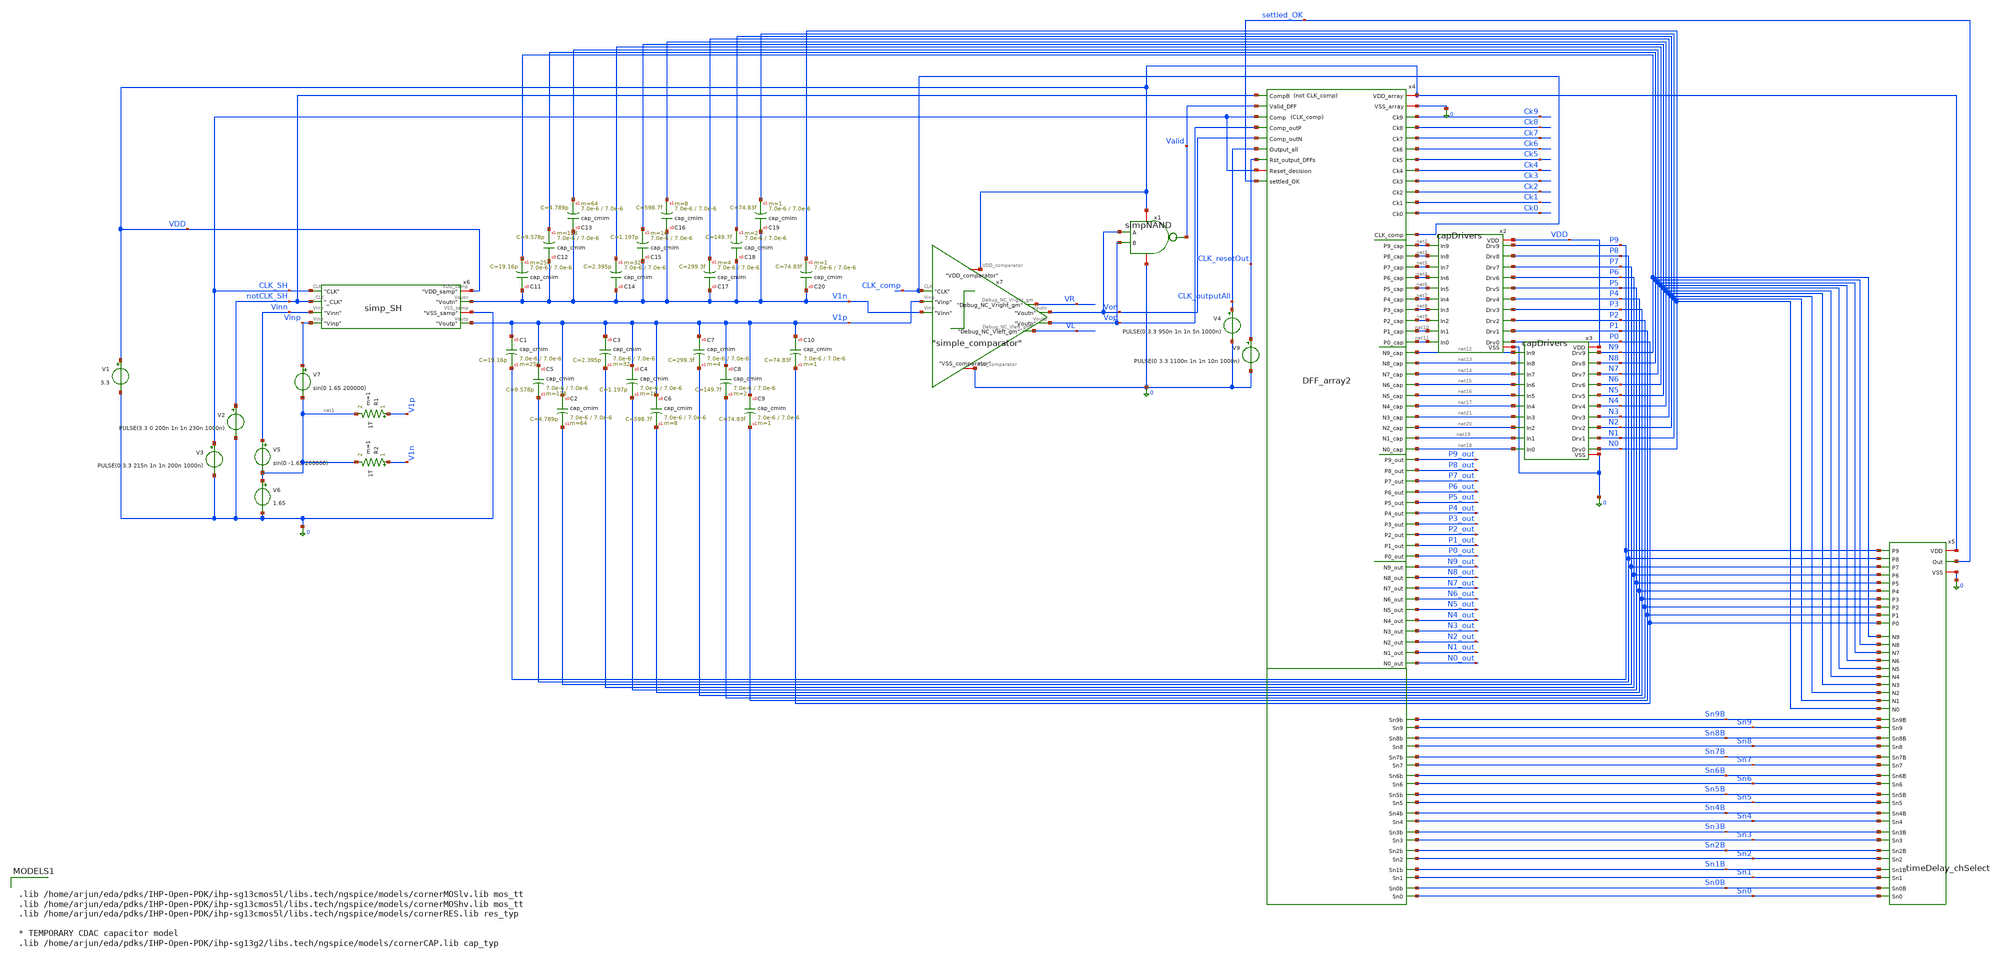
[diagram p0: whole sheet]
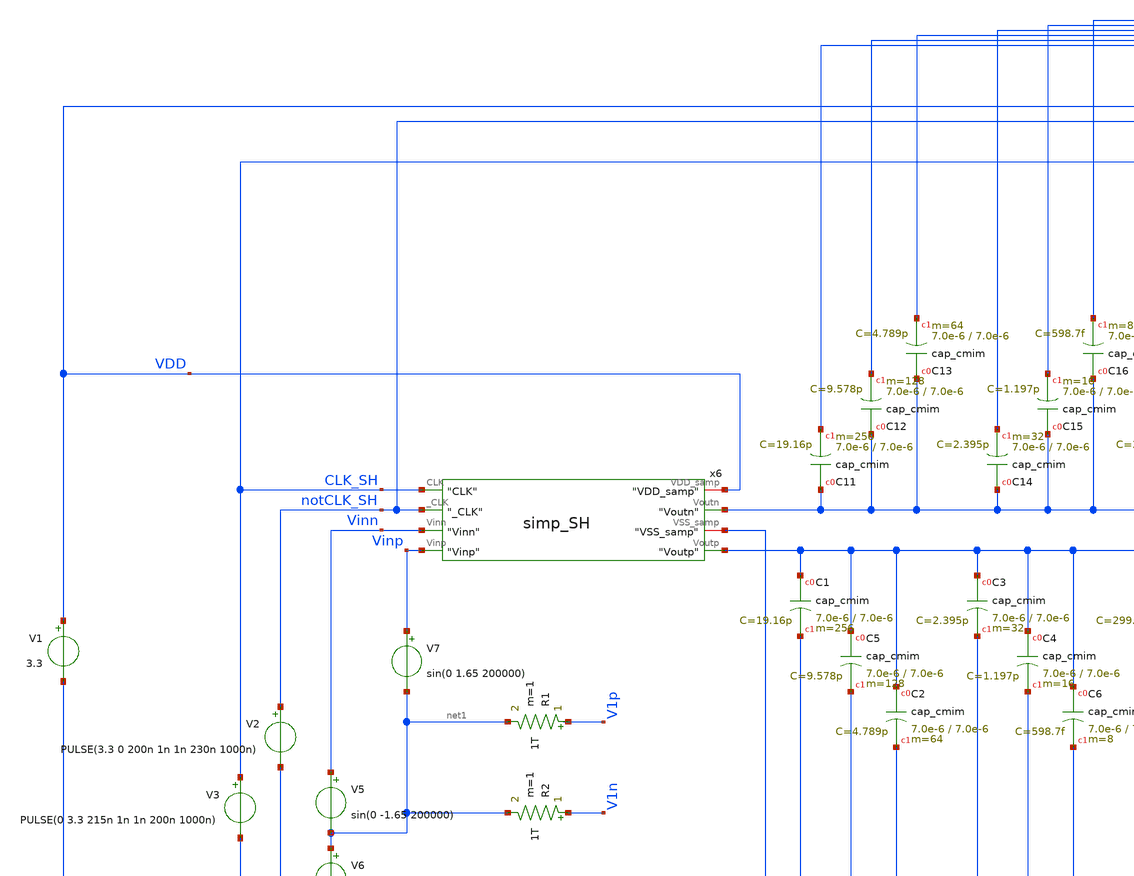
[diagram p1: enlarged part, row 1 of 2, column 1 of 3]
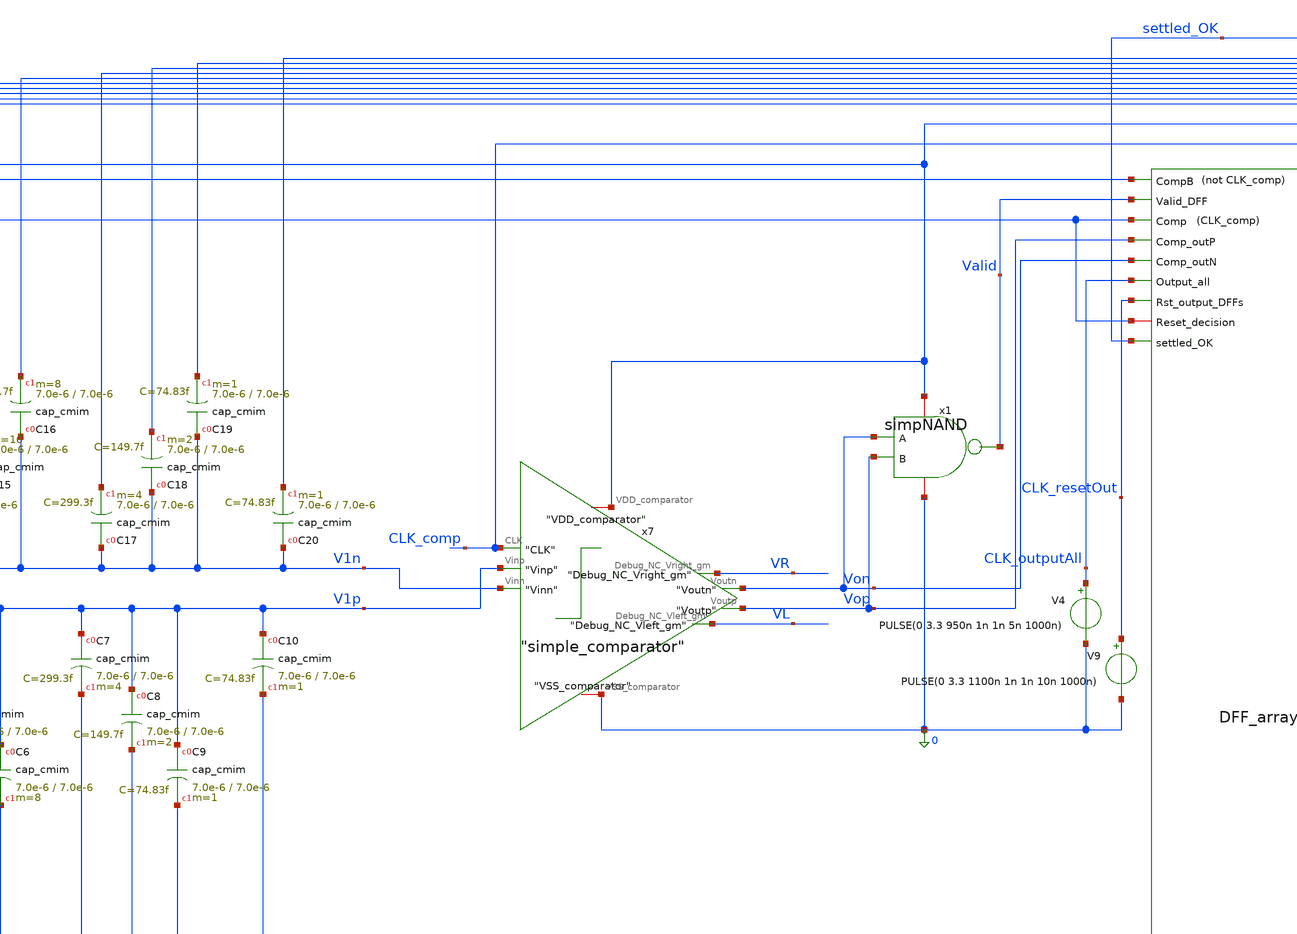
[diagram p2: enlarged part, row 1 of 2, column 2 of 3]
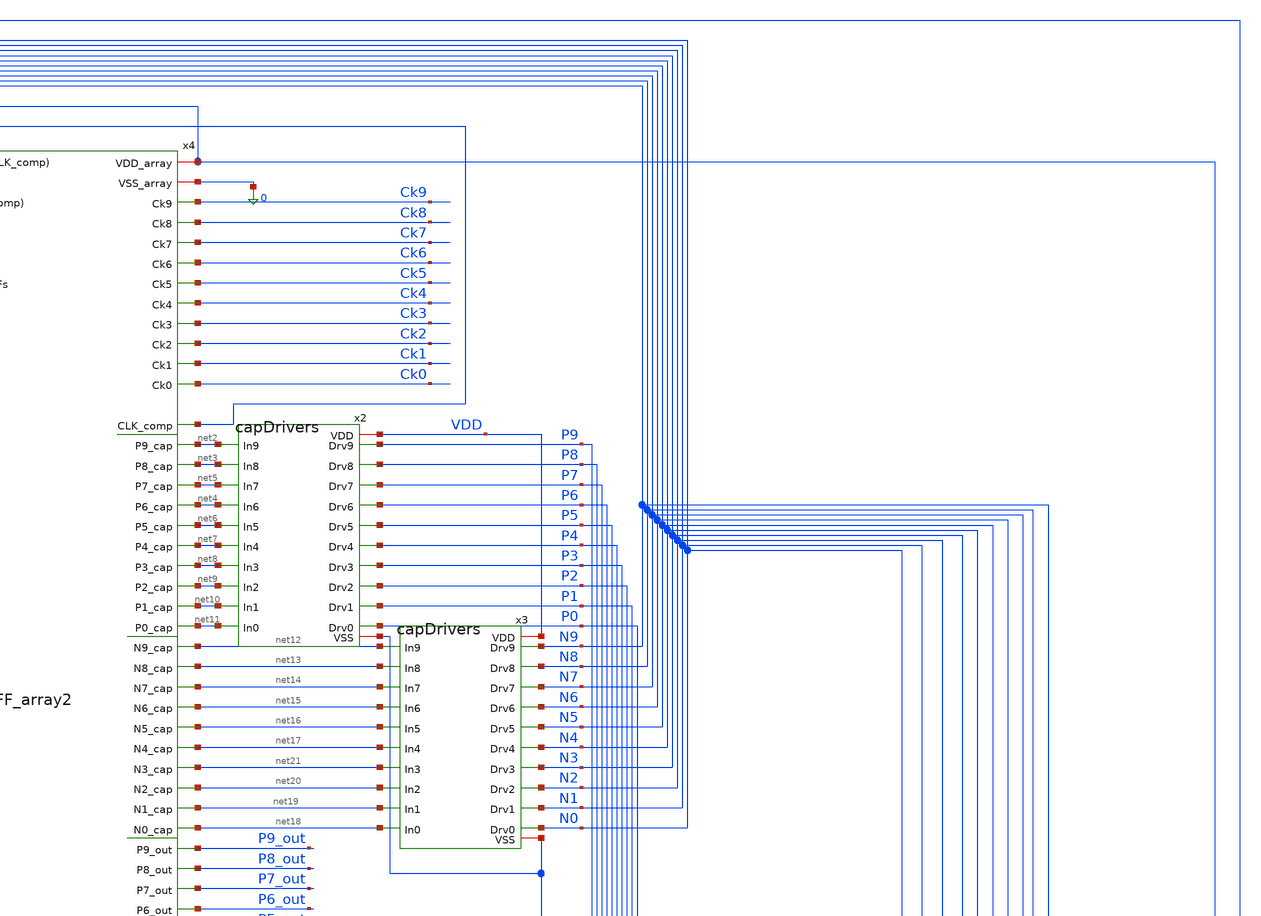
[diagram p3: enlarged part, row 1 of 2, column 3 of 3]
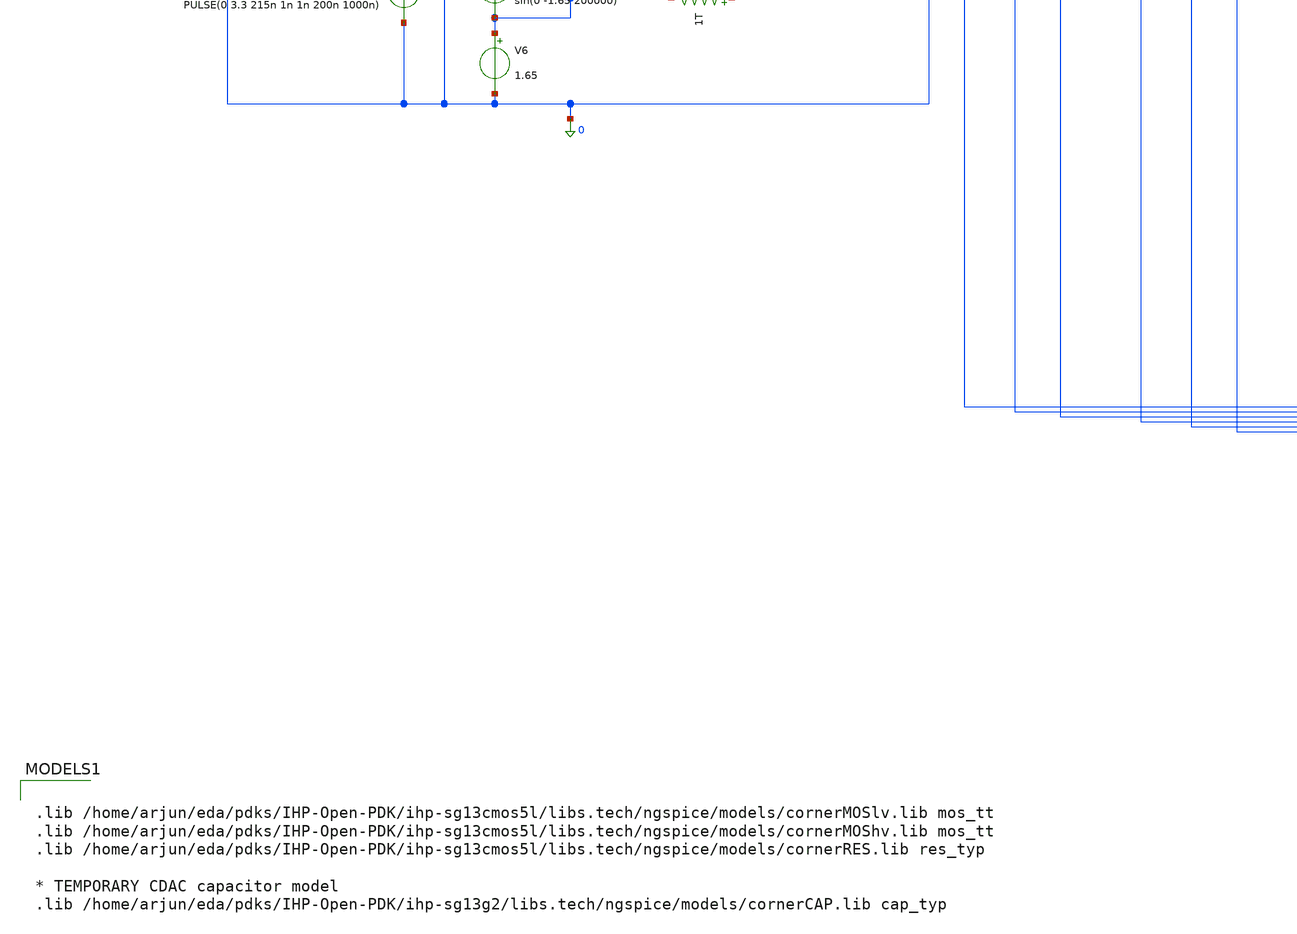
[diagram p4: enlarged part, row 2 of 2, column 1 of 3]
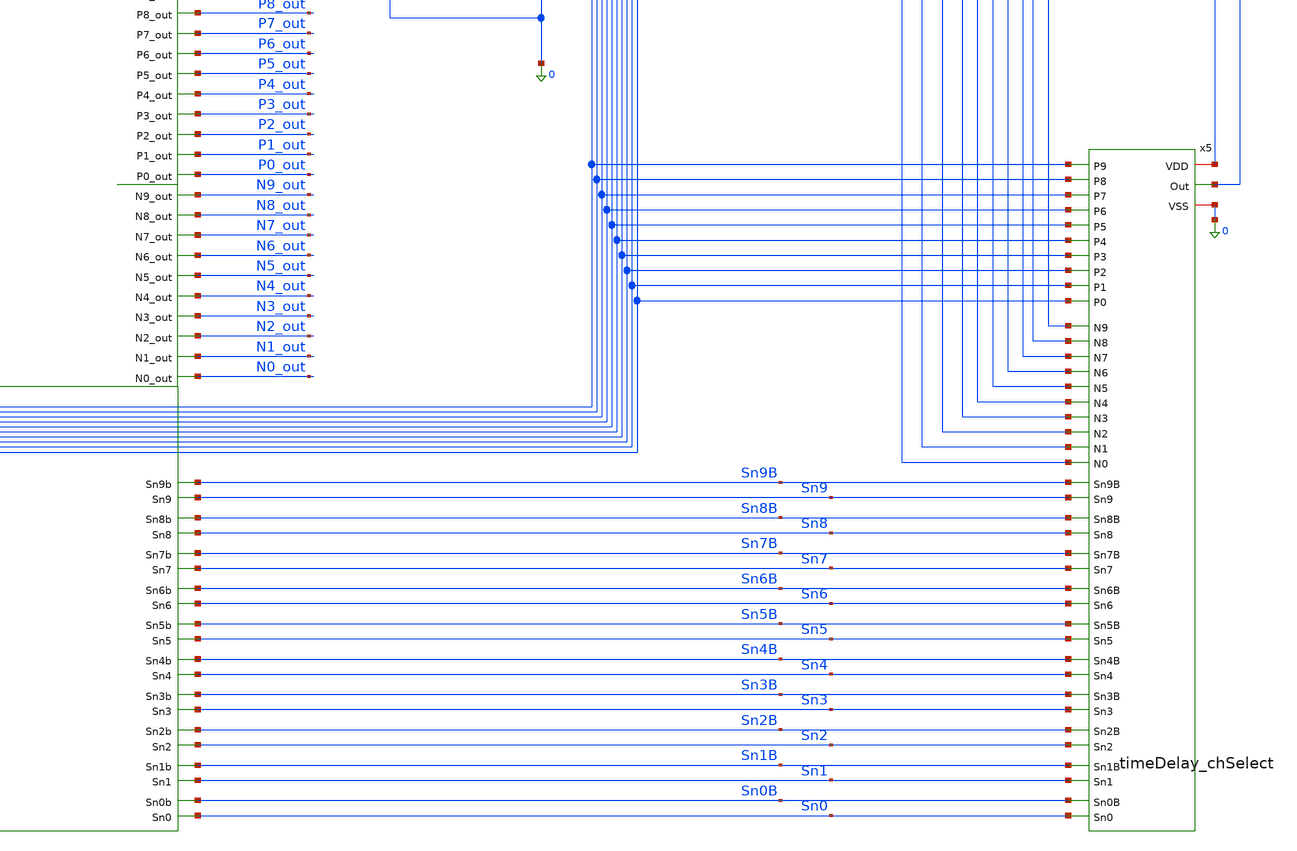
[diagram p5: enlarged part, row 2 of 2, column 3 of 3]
** sch_path: circuit_files/xschem_symbols/upper_TB.sch
**.subckt upper_TB
V2 notCLK_SH 0 PULSE(3.3 0 200n 1n 1n 230n 1000n)
V5 Vinn net1 sin(0 -1.65 200000)
V6 net1 0 1.65
V7 Vinp net1 sin(0 1.65 200000)
V3 CLK_SH 0 PULSE(0 3.3 215n 1n 1n 200n 1000n)
XC1 V1p P9 cap_cmim w=7.0e-6 l=7.0e-6 m=256 mm_ok=1
XC5 V1p P8 cap_cmim w=7.0e-6 l=7.0e-6 m=128 mm_ok=1
XC2 V1p P7 cap_cmim w=7.0e-6 l=7.0e-6 m=64 mm_ok=1
XC3 V1p P6 cap_cmim w=7.0e-6 l=7.0e-6 m=32 mm_ok=1
XC4 V1p P5 cap_cmim w=7.0e-6 l=7.0e-6 m=16 mm_ok=1
XC6 V1p P4 cap_cmim w=7.0e-6 l=7.0e-6 m=8 mm_ok=1
XC7 V1p P3 cap_cmim w=7.0e-6 l=7.0e-6 m=4 mm_ok=1
XC8 V1p P2 cap_cmim w=7.0e-6 l=7.0e-6 m=2 mm_ok=1
XC9 V1p P1 cap_cmim w=7.0e-6 l=7.0e-6 m=1 mm_ok=1
XC10 V1p P0 cap_cmim w=7.0e-6 l=7.0e-6 m=1 mm_ok=1
XC11 V1n N9 cap_cmim w=7.0e-6 l=7.0e-6 m=256 mm_ok=1
XC12 V1n N8 cap_cmim w=7.0e-6 l=7.0e-6 m=128 mm_ok=1
XC13 V1n N7 cap_cmim w=7.0e-6 l=7.0e-6 m=64 mm_ok=1
XC14 V1n N6 cap_cmim w=7.0e-6 l=7.0e-6 m=32 mm_ok=1
XC15 V1n N5 cap_cmim w=7.0e-6 l=7.0e-6 m=16 mm_ok=1
XC16 V1n N4 cap_cmim w=7.0e-6 l=7.0e-6 m=8 mm_ok=1
XC17 V1n N3 cap_cmim w=7.0e-6 l=7.0e-6 m=4 mm_ok=1
XC18 V1n N2 cap_cmim w=7.0e-6 l=7.0e-6 m=2 mm_ok=1
XC19 V1n N1 cap_cmim w=7.0e-6 l=7.0e-6 m=1 mm_ok=1
XC20 V1n N0 cap_cmim w=7.0e-6 l=7.0e-6 m=1 mm_ok=1
V4 CLK_outputAll 0 PULSE(0 3.3 950n 1n 1n 5n 1000n)
V9 CLK_resetOut 0 PULSE(0 3.3 1100n 1n 1n 10n 1000n)
V1 VDD 0 3.3
x6 VDD CLK_SH V1n notCLK_SH Vinn 0 V1p Vinp simp_SH
x7 VDD CLK_comp Von Vop VR VL V1p V1n 0 simple_comparator
x1 VDD Valid Von Vop 0 simpNAND
x2 VDD P9 net2 P8 net3 P7 net5 P6 net4 P5 net6 net7 P4 P3 net8 net9 P2 net10 P1 P0 net11 0
+ capDrivers
x4 Sn9B Sn7B Sn4B Sn6B Sn0B Sn3B Sn2B Sn5B Sn8B Sn1B Sn0 Sn4 Sn9 Sn6 Sn5 Sn8 Sn3 Sn7 Sn1 Sn2 VDD
+ notCLK_SH Valid 0 Ck2 Ck8 Ck3 Ck9 Ck1 Ck0 Ck4 Ck6 Ck7 Ck5 CLK_SH CLK_SH Vop CLK_comp net2 net3 net5 net4 net6
+ net7 net8 net9 net10 net11 Von net12 net13 net14 net15 net16 net17 net21 net20 net19 net18 P9_out P8_out
+ P7_out P6_out P5_out P4_out P3_out P2_out P1_out P0_out CLK_outputAll CLK_resetOut N9_out N8_out N7_out
+ N6_out N5_out N4_out N3_out N2_out N1_out N0_out settled_OK DFF_array2
x3 VDD N9 net12 N8 net13 N7 net14 N6 net15 N5 net16 net17 N4 N3 net21 net20 N2 net19 N1 N0 net18 0
+ capDrivers
x5 Sn8B Sn9B P5 P6 P9 P7 P8 VDD Sn9 Sn5 Sn7B Sn6B Sn5B N9 N6 N5 N8 N7 Sn8 Sn7 Sn6 Sn4B settled_OK P1
+ P0 P2 P3 P4 0 Sn0 Sn1 Sn2 Sn3 Sn0B Sn1B Sn2B Sn3B N0 N1 N2 N3 N4 Sn4 timeDelay_chSelect
R1 V1p net1 1T m=1
R2 V1n net1 1T m=1
**** begin user architecture code



.param temp=27

.save v(CLK_SH) v(notCLK_SH) v(CLK_outputAll) v(CLK_resetOut) v(CLK_comp) v(CLK_compB) v(CLK_compB_prebuff)
.save v(Vinp) v(Vinn) v(v1p) v(V1n)
.save v(Von) v(Vop) v(Valid) v(settled_OK)
.save v(Ck9) v(Ck8) v(Ck7) v(Ck6) v(Ck5) v(Ck4) v(Ck3) v(Ck2) v(Ck1) v(Ck0)

.save v(Sn9) v(Sn8) v(Sn7) v(Sn6) v(Sn5) v(Sn4) v(Sn3) v(Sn2) v(Sn1) v(Sn0)
.save v(Sn9B) v(Sn8B) v(Sn7B) v(Sn6B) v(Sn5B) v(Sn4B) v(Sn3B) v(Sn2B) v(Sn1B) v(Sn0B)

.save v(P9) v(P8) v(P7) v(P6) v(P5) v(P4) v(P3) v(P2) v(P1) v(P0)
.save v(N9) v(N8) v(N7) v(N6) v(N5) v(N4) v(N3) v(N2) v(N1) v(N0)
.save v(P9_out) v(P8_out) v(P7_out) v(P6_out) v(P5_out) v(P4_out) v(P3_out) v(P2_out) v(P1_out) v(P0_out)
.save v(N9_out) v(N8_out) v(N7_out) v(N6_out) v(N5_out) v(N4_out) v(N3_out) v(N2_out) v(N1_out) v(N0_out)
.save v(x4.x27.net3)
.save v(x4.x36.net3)
.save v(x4.x48.net3)
.save v(x4.x47.net2)
.save v(x4.x27.net1)
.save v(x4.x27.net2)
.save v(x4.x27.net3)
.save v(x4.x27.net4)
.save v(x4.x27.net5)
.save v(x4.x27.net7)
.save v(x4.x27.net8)
.save v(x4.x27.net9)

.ic v(P9) = 0
.ic v(P8) = 0
.ic v(P7) = 0
.ic v(P6) = 0
.ic v(P5) = 0
.ic v(P4) = 0
.ic v(P3) = 0
.ic v(P2) = 0
.ic v(P1) = 0
.ic v(P0) = 0

.ic v(N9) = 0
.ic v(N8) = 0
.ic v(N7) = 0
.ic v(N6) = 0
.ic v(N5) = 0
.ic v(N4) = 0
.ic v(N3) = 0
.ic v(N2) = 0
.ic v(N1) = 0
.ic v(N0) = 0

.ic v(V1p) = 1.65
.ic v(V1n) = 1.65

.ic v(x1.clk_pnot) = 0
.tran 0.1n 1300n

.control
set num_threads 1
run
write testWhole_debug_noValid.raw
.endc



.lib /home/arjun/eda/pdks/IHP-Open-PDK/ihp-sg13cmos5l/libs.tech/ngspice/models/cornerMOSlv.lib mos_tt
.lib /home/arjun/eda/pdks/IHP-Open-PDK/ihp-sg13cmos5l/libs.tech/ngspice/models/cornerMOShv.lib mos_tt
.lib /home/arjun/eda/pdks/IHP-Open-PDK/ihp-sg13cmos5l/libs.tech/ngspice/models/cornerRES.lib res_typ

* TEMPORARY CDAC capacitor model
.lib /home/arjun/eda/pdks/IHP-Open-PDK/ihp-sg13g2/libs.tech/ngspice/models/cornerCAP.lib cap_typ

**** end user architecture code
**.ends
.end
